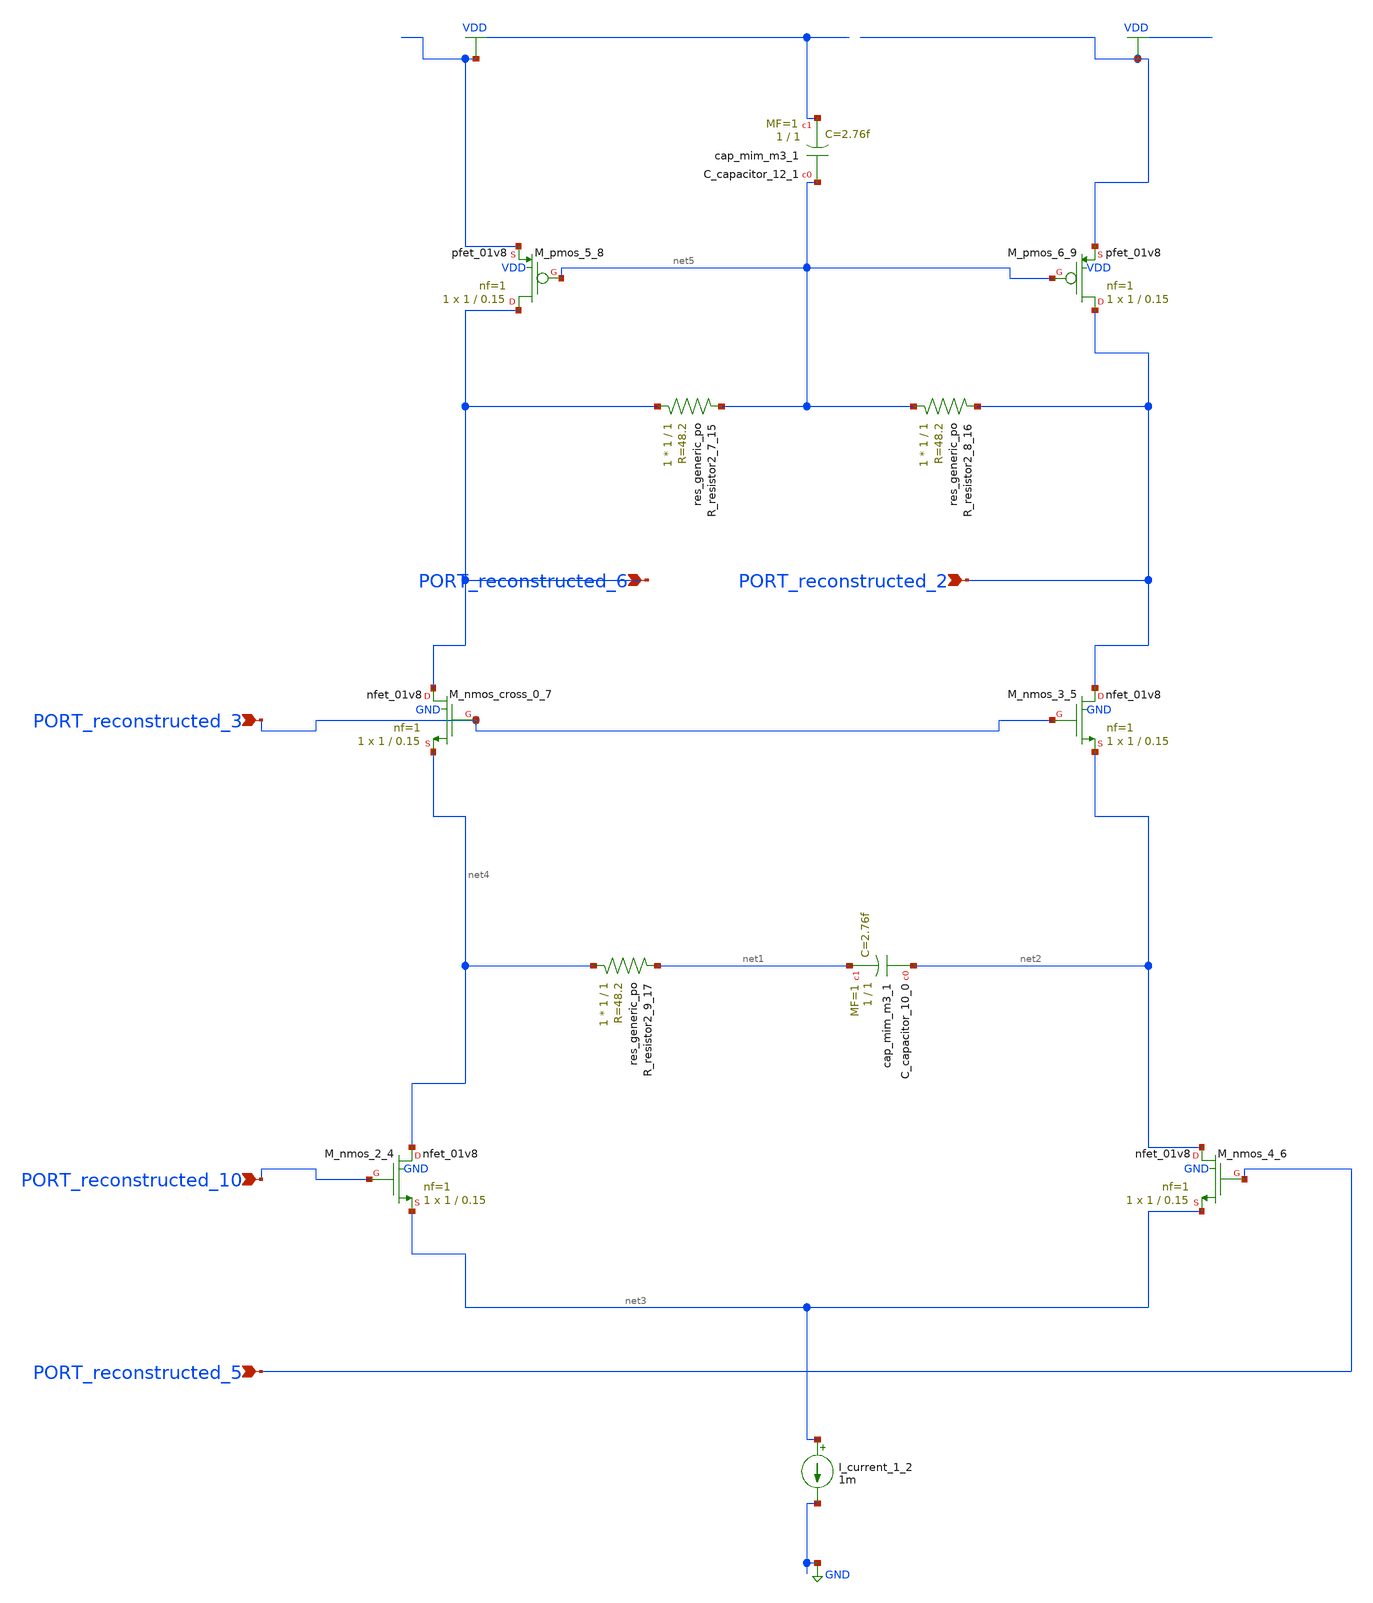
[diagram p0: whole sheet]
** sch_path: schematics/AMSNet/422.sch
**.subckt 422 PORT_reconstructed_6 PORT_reconstructed_3 PORT_reconstructed_2 PORT_reconstructed_5
*+ PORT_reconstructed_10
*.ipin PORT_reconstructed_6
*.ipin PORT_reconstructed_3
*.ipin PORT_reconstructed_2
*.ipin PORT_reconstructed_5
*.ipin PORT_reconstructed_10
XC_capacitor_10_0 net2 net1 sky130_fd_pr__cap_mim_m3_1 W=1 L=1 MF=1 m=1
XC_capacitor_12_1 net5 VDD sky130_fd_pr__cap_mim_m3_1 W=1 L=1 MF=1 m=1
I_current_1_2 net3 GND 1m
XM_nmos_2_4 net4 PORT_reconstructed_10 net3 GND sky130_fd_pr__nfet_01v8 L=0.15 W=1 nf=1 ad='int((1 + 1)/2) * 1 / 1 * 0.29'
+ as='int((1 + 2)/2) * 1 / 1 * 0.29' pd='2*int((1 + 1)/2) * (1 / 1 + 0.29)' ps='2*int((1 + 2)/2) * (1 / 1 + 0.29)'
+ nrd='0.29 / 1 ' nrs='0.29 / 1 ' sa=0 sb=0 sd=0 mult=1 m=1
XM_nmos_3_5 PORT_reconstructed_2 PORT_reconstructed_3 net2 GND sky130_fd_pr__nfet_01v8 L=0.15 W=1 nf=1
+ ad='int((1 + 1)/2) * 1 / 1 * 0.29' as='int((1 + 2)/2) * 1 / 1 * 0.29' pd='2*int((1 + 1)/2) * (1 / 1 + 0.29)'
+ ps='2*int((1 + 2)/2) * (1 / 1 + 0.29)' nrd='0.29 / 1 ' nrs='0.29 / 1 ' sa=0 sb=0 sd=0 mult=1 m=1
XM_nmos_4_6 net2 PORT_reconstructed_5 net3 GND sky130_fd_pr__nfet_01v8 L=0.15 W=1 nf=1 ad='int((1 + 1)/2) * 1 / 1 * 0.29'
+ as='int((1 + 2)/2) * 1 / 1 * 0.29' pd='2*int((1 + 1)/2) * (1 / 1 + 0.29)' ps='2*int((1 + 2)/2) * (1 / 1 + 0.29)'
+ nrd='0.29 / 1 ' nrs='0.29 / 1 ' sa=0 sb=0 sd=0 mult=1 m=1
XM_nmos_cross_0_7 PORT_reconstructed_6 PORT_reconstructed_3 net4 GND sky130_fd_pr__nfet_01v8 L=0.15 W=1
+ nf=1 ad='int((1 + 1)/2) * 1 / 1 * 0.29' as='int((1 + 2)/2) * 1 / 1 * 0.29' pd='2*int((1 + 1)/2) * (1 / 1 + 0.29)'
+ ps='2*int((1 + 2)/2) * (1 / 1 + 0.29)' nrd='0.29 / 1 ' nrs='0.29 / 1 ' sa=0 sb=0 sd=0 mult=1 m=1
XM_pmos_5_8 PORT_reconstructed_6 net5 VDD VDD sky130_fd_pr__pfet_01v8 L=0.15 W=1 nf=1 ad='int((1 + 1)/2) * 1 / 1 * 0.29'
+ as='int((1 + 2)/2) * 1 / 1 * 0.29' pd='2*int((1 + 1)/2) * (1 / 1 + 0.29)' ps='2*int((1 + 2)/2) * (1 / 1 + 0.29)'
+ nrd='0.29 / 1 ' nrs='0.29 / 1 ' sa=0 sb=0 sd=0 mult=1 m=1
XM_pmos_6_9 PORT_reconstructed_2 net5 VDD VDD sky130_fd_pr__pfet_01v8 L=0.15 W=1 nf=1 ad='int((1 + 1)/2) * 1 / 1 * 0.29'
+ as='int((1 + 2)/2) * 1 / 1 * 0.29' pd='2*int((1 + 1)/2) * (1 / 1 + 0.29)' ps='2*int((1 + 2)/2) * (1 / 1 + 0.29)'
+ nrd='0.29 / 1 ' nrs='0.29 / 1 ' sa=0 sb=0 sd=0 mult=1 m=1
XR_resistor2_7_15 PORT_reconstructed_6 net5 sky130_fd_pr__res_generic_po W=1 L=1 m=1
XR_resistor2_8_16 net5 PORT_reconstructed_2 sky130_fd_pr__res_generic_po W=1 L=1 m=1
XR_resistor2_9_17 net4 net1 sky130_fd_pr__res_generic_po W=1 L=1 m=1
**.ends
.GLOBAL GND
.GLOBAL VDD
.end
